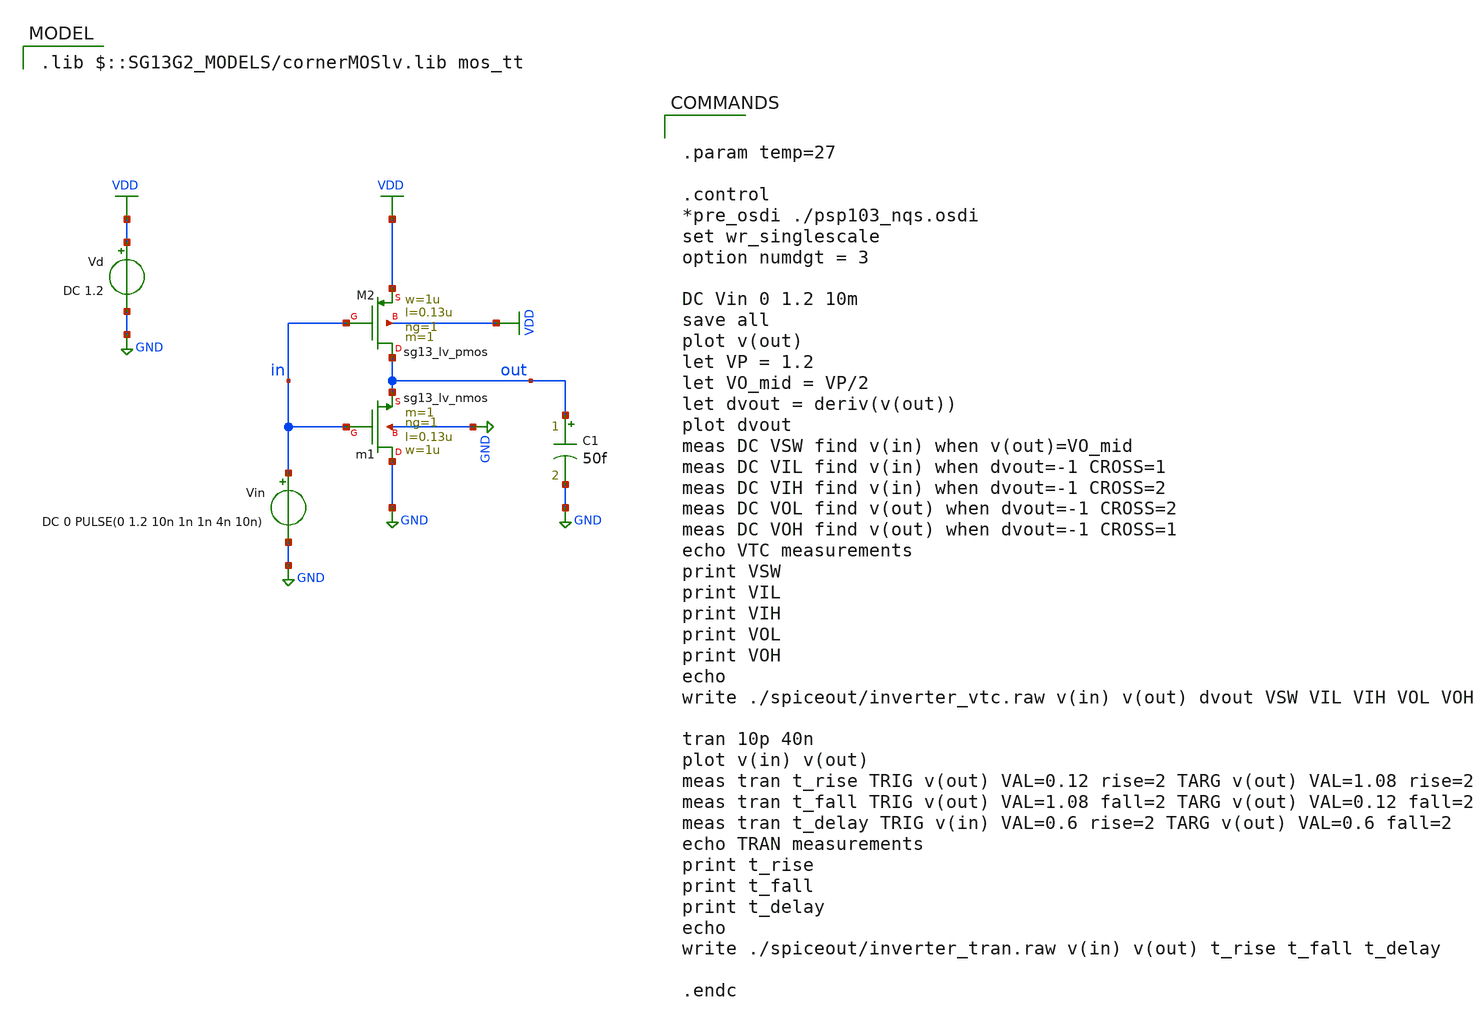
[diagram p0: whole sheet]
** sch_path: 04_cmos_inverter/src/inverter.sch
**.subckt inverter
Xm1 GND in out GND sg13_lv_nmos w=1u l=0.13u ng=1 m=1 mm_ok=1
Vin in GND DC 0 PULSE(0 1.2 10n 1n 1n 4n 10n)
XM2 out in VDD VDD sg13_lv_pmos w=1u l=0.13u ng=1 m=1 mm_ok=1
Vd VDD GND DC 1.2
C1 out GND 50f m=1
**** begin user architecture code
 .lib $::SG13G2_MODELS/cornerMOSlv.lib mos_tt



.param temp=27

.control
*pre_osdi ./psp103_nqs.osdi
set wr_singlescale
option numdgt = 3

DC Vin 0 1.2 10m
save all
plot v(out)
let VP = 1.2
let VO_mid = VP/2
let dvout = deriv(v(out))
plot dvout
meas DC VSW find v(in) when v(out)=VO_mid
meas DC VIL find v(in) when dvout=-1 CROSS=1
meas DC VIH find v(in) when dvout=-1 CROSS=2
meas DC VOL find v(out) when dvout=-1 CROSS=2
meas DC VOH find v(out) when dvout=-1 CROSS=1
echo VTC measurements
print VSW
print VIL
print VIH
print VOL
print VOH
echo
write ./spiceout/inverter_vtc.raw v(in) v(out) dvout VSW VIL VIH VOL VOH

tran 10p 40n
plot v(in) v(out)
meas tran t_rise TRIG v(out) VAL=0.12 rise=2 TARG v(out) VAL=1.08 rise=2
meas tran t_fall TRIG v(out) VAL=1.08 fall=2 TARG v(out) VAL=0.12 fall=2
meas tran t_delay TRIG v(in) VAL=0.6 rise=2 TARG v(out) VAL=0.6 fall=2
echo TRAN measurements
print t_rise
print t_fall
print t_delay
echo
write ./spiceout/inverter_tran.raw v(in) v(out) t_rise t_fall t_delay

.endc


**** end user architecture code
**.ends
.GLOBAL GND
.GLOBAL VDD
.end
